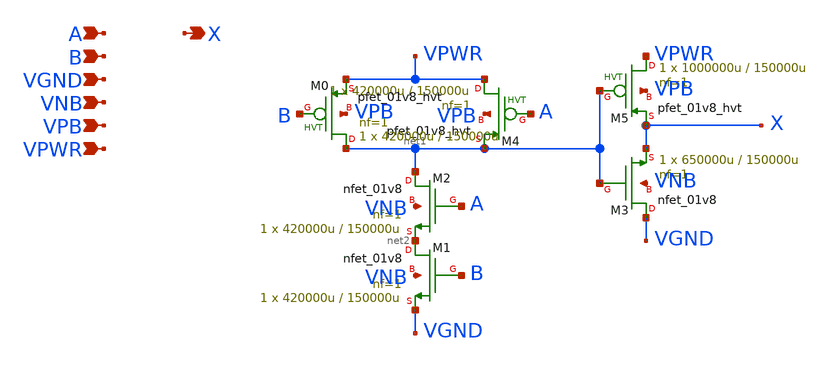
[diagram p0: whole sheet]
** sch_path: schematics/and2/sky130_fd_sc_hd__and2_1.sch
**.subckt sky130_fd_sc_hd__and2_1 A X B VGND VNB VPB VPWR
*.ipin A
*.opin X
*.ipin B
*.ipin VGND
*.ipin VNB
*.ipin VPB
*.ipin VPWR
XM4 VPWR A net1 VPB sky130_fd_pr__pfet_01v8_hvt L=150000u W=420000u nf=1 ad='int((1 + 1)/2) * 420000u / 1 * 0.29'
+ as='int((1 + 2)/2) * 420000u / 1 * 0.29' pd='2*int((1 + 1)/2) * (420000u / 1 + 0.29)' ps='2*int((1 + 2)/2) * (420000u / 1 + 0.29)'
+ nrd='0.29 / 420000u ' nrs='0.29 / 420000u ' sa=0 sb=0 sd=0 mult=1 m=1
XM0 net1 B VPWR VPB sky130_fd_pr__pfet_01v8_hvt L=150000u W=420000u nf=1 ad='int((1 + 1)/2) * 420000u / 1 * 0.29'
+ as='int((1 + 2)/2) * 420000u / 1 * 0.29' pd='2*int((1 + 1)/2) * (420000u / 1 + 0.29)' ps='2*int((1 + 2)/2) * (420000u / 1 + 0.29)'
+ nrd='0.29 / 420000u ' nrs='0.29 / 420000u ' sa=0 sb=0 sd=0 mult=1 m=1
XM2 net1 A net2 VNB sky130_fd_pr__nfet_01v8 L=150000u W=420000u nf=1 ad='int((1 + 1)/2) * 420000u / 1 * 0.29'
+ as='int((1 + 2)/2) * 420000u / 1 * 0.29' pd='2*int((1 + 1)/2) * (420000u / 1 + 0.29)' ps='2*int((1 + 2)/2) * (420000u / 1 + 0.29)'
+ nrd='0.29 / 420000u ' nrs='0.29 / 420000u ' sa=0 sb=0 sd=0 mult=1 m=1
XM1 net2 B VGND VNB sky130_fd_pr__nfet_01v8 L=150000u W=420000u nf=1 ad='int((1 + 1)/2) * 420000u / 1 * 0.29'
+ as='int((1 + 2)/2) * 420000u / 1 * 0.29' pd='2*int((1 + 1)/2) * (420000u / 1 + 0.29)' ps='2*int((1 + 2)/2) * (420000u / 1 + 0.29)'
+ nrd='0.29 / 420000u ' nrs='0.29 / 420000u ' sa=0 sb=0 sd=0 mult=1 m=1
XM3 VGND net1 X VNB sky130_fd_pr__nfet_01v8 L=150000u W=650000u nf=1 ad='int((1 + 1)/2) * 650000u / 1 * 0.29'
+ as='int((1 + 2)/2) * 650000u / 1 * 0.29' pd='2*int((1 + 1)/2) * (650000u / 1 + 0.29)' ps='2*int((1 + 2)/2) * (650000u / 1 + 0.29)'
+ nrd='0.29 / 650000u ' nrs='0.29 / 650000u ' sa=0 sb=0 sd=0 mult=1 m=1
XM5 VPWR net1 X VPB sky130_fd_pr__pfet_01v8_hvt L=150000u W=1000000u nf=1 ad='int((1 + 1)/2) * 1000000u / 1 * 0.29'
+ as='int((1 + 2)/2) * 1000000u / 1 * 0.29' pd='2*int((1 + 1)/2) * (1000000u / 1 + 0.29)' ps='2*int((1 + 2)/2) * (1000000u / 1 + 0.29)'
+ nrd='0.29 / 1000000u ' nrs='0.29 / 1000000u ' sa=0 sb=0 sd=0 mult=1 m=1
**.ends
.end
